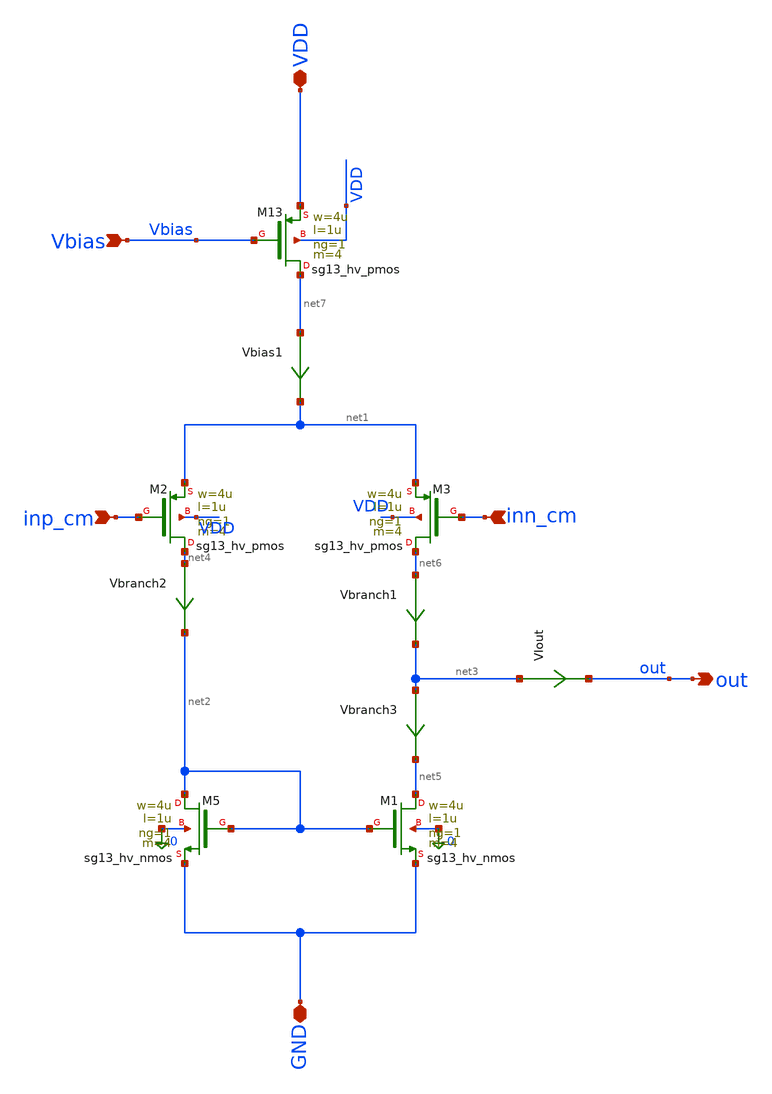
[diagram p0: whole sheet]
** sch_path: xschem/V2I_final.sch
**.subckt V2I_final inn_cm inp_cm out Vbias VDD GND
*.ipin inn_cm
*.ipin inp_cm
*.opin out
*.ipin Vbias
*.iopin VDD
*.iopin GND
VIout net3 out 0
.save i(viout)
XM2 net4 inp_cm net1 VDD sg13_hv_pmos w=4u l=1u ng=1 m=4 mm_ok=1
XM5 net2 net2 GND 0 sg13_hv_nmos w=4u l=1u ng=1 m=4 mm_ok=1
Vbias1 net7 net1 0
.save i(vbias1)
Vbranch1 net6 net3 0
.save i(vbranch1)
Vbranch2 net4 net2 0
.save i(vbranch2)
Vbranch3 net3 net5 0
.save i(vbranch3)
XM13 net7 Vbias VDD VDD sg13_hv_pmos w=4u l=1u ng=1 m=4 mm_ok=1
XM1 net5 net2 GND 0 sg13_hv_nmos w=4u l=1u ng=1 m=4 mm_ok=1
XM3 net6 inn_cm net1 VDD sg13_hv_pmos w=4u l=1u ng=1 m=4 mm_ok=1
**.ends
.end
